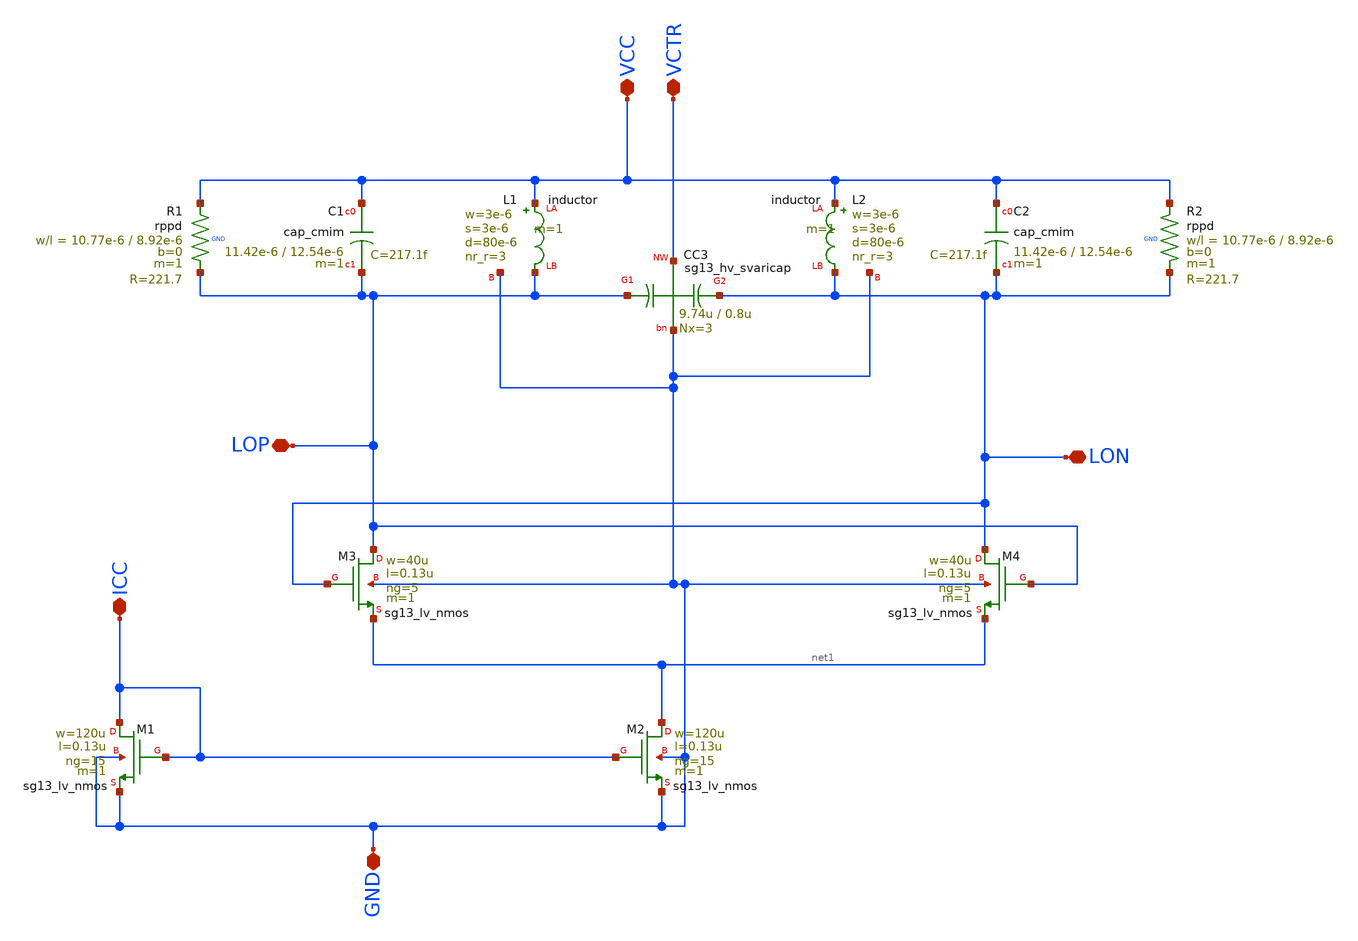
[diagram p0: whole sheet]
** sch_path: schematic/xschem/cryoVCO.sch
**.subckt cryoVCO VCC LOP GND VCTR ICC LON
*.iopin VCC
*.iopin LOP
*.iopin GND
*.iopin VCTR
*.iopin ICC
*.iopin LON
XL1 VCC LOP GND inductor w=3e-6 s=3e-6 d=80e-6 nr_r=3 m=1
XR1 VCC LOP GND rppd w=10.77e-6 l=8.92e-6 m=1 b=0 mm_ok=1
XC1 VCC LOP cap_cmim w=11.42e-6 l=12.54e-6 m=1 mm_ok=1
XL2 VCC LON GND inductor w=3e-6 s=3e-6 d=80e-6 nr_r=3 m=1
XR2 VCC LON GND rppd w=10.77e-6 l=8.92e-6 m=1 b=0 mm_ok=1
XC2 VCC LON cap_cmim w=11.42e-6 l=12.54e-6 m=1 mm_ok=1
XC3 LOP VCTR LON GND sg13_hv_svaricap w=9.74u l=0.8u Nx=3
XM3 LOP LON net1 GND sg13_lv_nmos w=40u l=0.13u ng=5 m=1 mm_ok=1
XM4 LON LOP net1 GND sg13_lv_nmos w=40u l=0.13u ng=5 m=1 mm_ok=1
XM2 net1 ICC GND GND sg13_lv_nmos w=120u l=0.13u ng=15 m=1 mm_ok=1
XM1 ICC ICC GND GND sg13_lv_nmos w=120u l=0.13u ng=15 m=1 mm_ok=1
**.ends
.end
